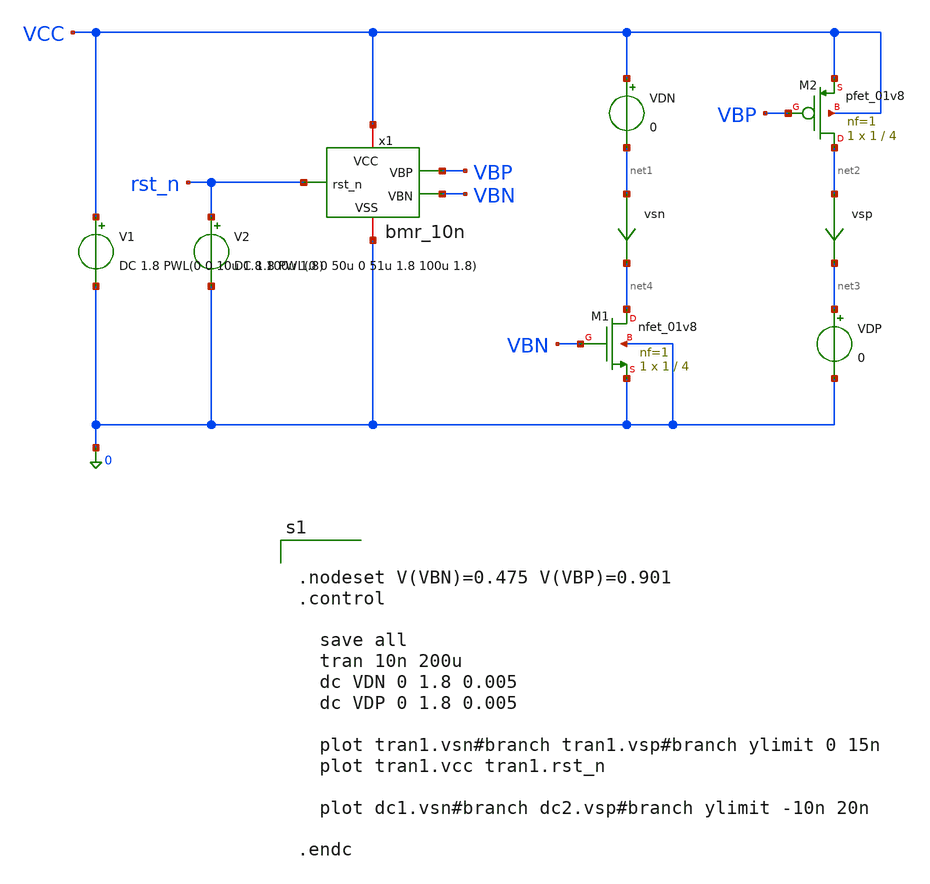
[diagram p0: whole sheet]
** sch_path: schem/bias/bmr_10n_tb.sch
**.subckt bmr_10n_tb
x1 VCC VBP 0 VBN rst_n bmr_10n
V1 VCC 0 DC 1.8 PWL(0 0 10u 1.8 100u 1.8)
V2 rst_n 0 DC 1.8 PWL(0 0 50u 0 51u 1.8 100u 1.8)
vsn net1 net4 0
.save i(vsn)
vsp net2 net3 0
.save i(vsp)
XM1 net4 VBN 0 0 sky130_fd_pr__nfet_01v8 L=4 W=1 nf=1 ad='int((1 + 1)/2) * 1 / 1 * 0.29' as='int((1 + 2)/2) * 1 / 1 * 0.29'
+ pd='2*int((1 + 1)/2) * (1 / 1 + 0.29)' ps='2*int((1 + 2)/2) * (1 / 1 + 0.29)' nrd='0.29 / 1 ' nrs='0.29 / 1 '
+ sa=0 sb=0 sd=0 mult=1 m=1
XM2 net2 VBP VCC VCC sky130_fd_pr__pfet_01v8 L=4 W=1 nf=1 ad='int((1 + 1)/2) * 1 / 1 * 0.29' as='int((1 + 2)/2) * 1 / 1 * 0.29'
+ pd='2*int((1 + 1)/2) * (1 / 1 + 0.29)' ps='2*int((1 + 2)/2) * (1 / 1 + 0.29)' nrd='0.29 / 1 ' nrs='0.29 / 1 '
+ sa=0 sb=0 sd=0 mult=1 m=1
VDN VCC net1 0
VDP net3 0 0
**** begin user architecture code

** opencircuitdesign pdks install
.lib $::SKYWATER_MODELS/sky130.lib.spice tt



.nodeset V(VBN)=0.475 V(VBP)=0.901
.control

  save all
  tran 10n 200u
  dc VDN 0 1.8 0.005
  dc VDP 0 1.8 0.005

  plot tran1.vsn#branch tran1.vsp#branch ylimit 0 15n
  plot tran1.vcc tran1.rst_n

  plot dc1.vsn#branch dc2.vsp#branch ylimit -10n 20n

.endc


**** end user architecture code
**.ends

* expanding   symbol:  bmr_10n.sym # of pins=5
** sym_path: schem/bias/bmr_10n.sym
** sch_path: schem/bias/bmr_10n.sch
.subckt bmr_10n VCC VBP VSS VBN rst_n
*.iopin VCC
*.iopin VSS
*.ipin rst_n
*.opin VBP
*.opin VBN
XM1 VBP VBP VCC VCC sky130_fd_pr__pfet_01v8 L=4 W=1 nf=1 ad='int((1 + 1)/2) * 1 / 1 * 0.29' as='int((1 + 2)/2) * 1 / 1 * 0.29'
+ pd='2*int((1 + 1)/2) * (1 / 1 + 0.29)' ps='2*int((1 + 2)/2) * (1 / 1 + 0.29)' nrd='0.29 / 1 ' nrs='0.29 / 1 '
+ sa=0 sb=0 sd=0 mult=1 m=1
XM2 net3 VBP VCC VCC sky130_fd_pr__pfet_01v8 L=4 W=1 nf=1 ad='int((1 + 1)/2) * 1 / 1 * 0.29' as='int((1 + 2)/2) * 1 / 1 * 0.29'
+ pd='2*int((1 + 1)/2) * (1 / 1 + 0.29)' ps='2*int((1 + 2)/2) * (1 / 1 + 0.29)' nrd='0.29 / 1 ' nrs='0.29 / 1 '
+ sa=0 sb=0 sd=0 mult=1 m=1
XM3 net2 VBN net1 VSS sky130_fd_pr__nfet_01v8 L=4 W=8 nf=1 ad='int((1 + 1)/2) * 8 / 1 * 0.29' as='int((1 + 2)/2) * 8 / 1 * 0.29'
+ pd='2*int((1 + 1)/2) * (8 / 1 + 0.29)' ps='2*int((1 + 2)/2) * (8 / 1 + 0.29)' nrd='0.29 / 8 ' nrs='0.29 / 8 '
+ sa=0 sb=0 sd=0 mult=1 m=1
XM4 VBN VBN VSS VSS sky130_fd_pr__nfet_01v8 L=4 W=1 nf=1 ad='int((1 + 1)/2) * 1 / 1 * 0.29' as='int((1 + 2)/2) * 1 / 1 * 0.29'
+ pd='2*int((1 + 1)/2) * (1 / 1 + 0.29)' ps='2*int((1 + 2)/2) * (1 / 1 + 0.29)' nrd='0.29 / 1 ' nrs='0.29 / 1 '
+ sa=0 sb=0 sd=0 mult=1 m=1
XR1 net5 net1 net4 sky130_fd_pr__res_xhigh_po_0p35 L={LR} mult=1 m=1
VSRIGHT VBP net2 0
.save i(vsright)
VSLEFT net3 VBN 0
.save i(vsleft)
XM5 VBN rst_n VCC VCC sky130_fd_pr__pfet_01v8 L=4 W=1 nf=1 ad='int((1 + 1)/2) * 1 / 1 * 0.29' as='int((1 + 2)/2) * 1 / 1 * 0.29'
+ pd='2*int((1 + 1)/2) * (1 / 1 + 0.29)' ps='2*int((1 + 2)/2) * (1 / 1 + 0.29)' nrd='0.29 / 1 ' nrs='0.29 / 1 '
+ sa=0 sb=0 sd=0 mult=1 m=1
XR2 net6 net5 net4 sky130_fd_pr__res_xhigh_po_0p35 L={LR} mult=1 m=1
XR3 net7 net6 net4 sky130_fd_pr__res_xhigh_po_0p35 L={LR} mult=1 m=1
XR4 net8 net7 net4 sky130_fd_pr__res_xhigh_po_0p35 L={LR} mult=1 m=1
XR5 net9 net8 net4 sky130_fd_pr__res_xhigh_po_0p35 L={LR} mult=1 m=1
XR6 net10 net9 net4 sky130_fd_pr__res_xhigh_po_0p35 L={LR} mult=1 m=1
XR7 net11 net10 net4 sky130_fd_pr__res_xhigh_po_0p35 L={LR} mult=1 m=1
XR8 VSS net11 net4 sky130_fd_pr__res_xhigh_po_0p35 L={LR} mult=1 m=1
**** begin user architecture code


.param LR=1084/8


**** end user architecture code
.ends

.end
